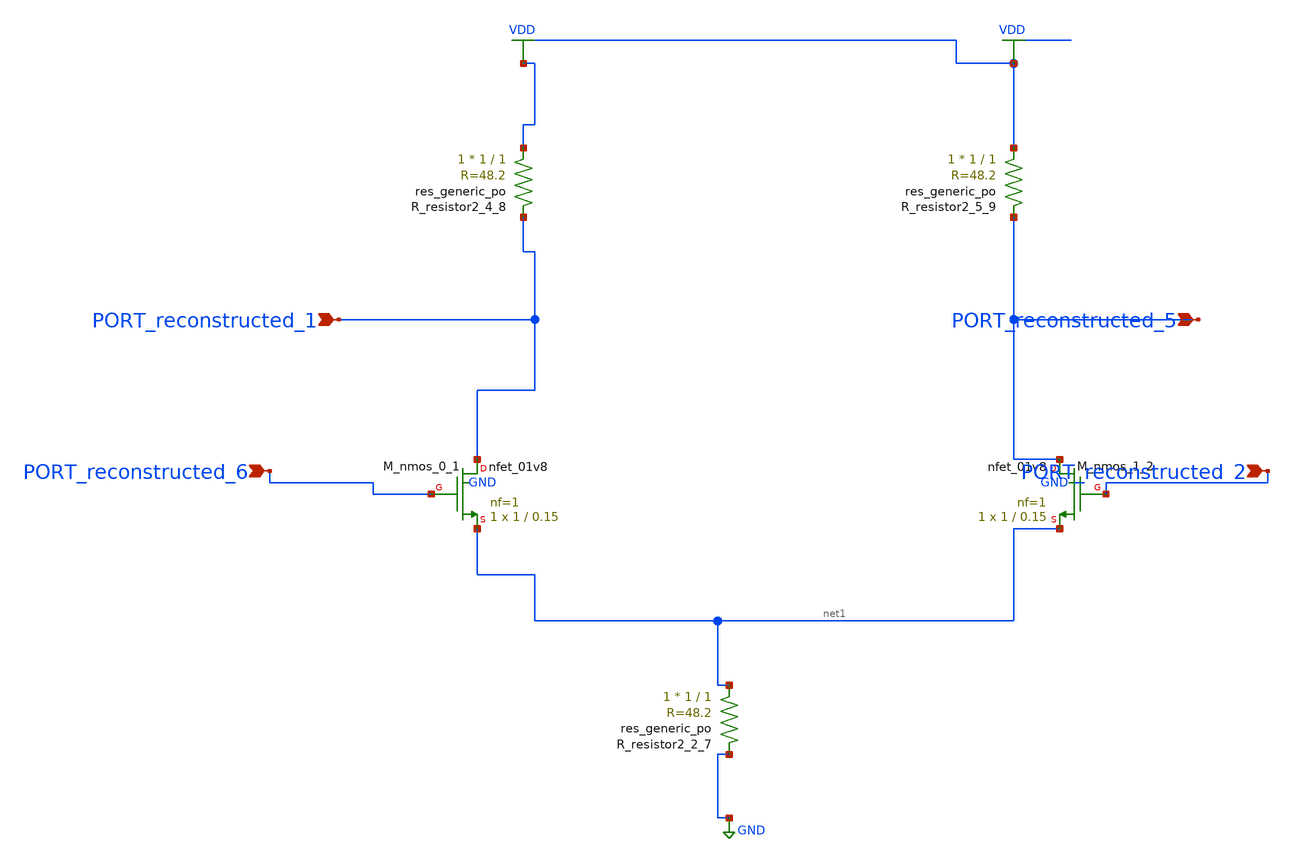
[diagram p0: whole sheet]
** sch_path: schematics/AMSNet/213.sch
**.subckt 213 PORT_reconstructed_1 PORT_reconstructed_5 PORT_reconstructed_6 PORT_reconstructed_2
*.ipin PORT_reconstructed_1
*.ipin PORT_reconstructed_5
*.ipin PORT_reconstructed_6
*.ipin PORT_reconstructed_2
XM_nmos_0_1 PORT_reconstructed_1 PORT_reconstructed_6 net1 GND sky130_fd_pr__nfet_01v8 L=0.15 W=1 nf=1
+ ad='int((1 + 1)/2) * 1 / 1 * 0.29' as='int((1 + 2)/2) * 1 / 1 * 0.29' pd='2*int((1 + 1)/2) * (1 / 1 + 0.29)'
+ ps='2*int((1 + 2)/2) * (1 / 1 + 0.29)' nrd='0.29 / 1 ' nrs='0.29 / 1 ' sa=0 sb=0 sd=0 mult=1 m=1
XM_nmos_1_2 PORT_reconstructed_5 PORT_reconstructed_2 net1 GND sky130_fd_pr__nfet_01v8 L=0.15 W=1 nf=1
+ ad='int((1 + 1)/2) * 1 / 1 * 0.29' as='int((1 + 2)/2) * 1 / 1 * 0.29' pd='2*int((1 + 1)/2) * (1 / 1 + 0.29)'
+ ps='2*int((1 + 2)/2) * (1 / 1 + 0.29)' nrd='0.29 / 1 ' nrs='0.29 / 1 ' sa=0 sb=0 sd=0 mult=1 m=1
XR_resistor2_2_7 net1 GND sky130_fd_pr__res_generic_po W=1 L=1 m=1
XR_resistor2_4_8 VDD PORT_reconstructed_1 sky130_fd_pr__res_generic_po W=1 L=1 m=1
XR_resistor2_5_9 VDD PORT_reconstructed_5 sky130_fd_pr__res_generic_po W=1 L=1 m=1
**.ends
.GLOBAL GND
.GLOBAL VDD
.end
